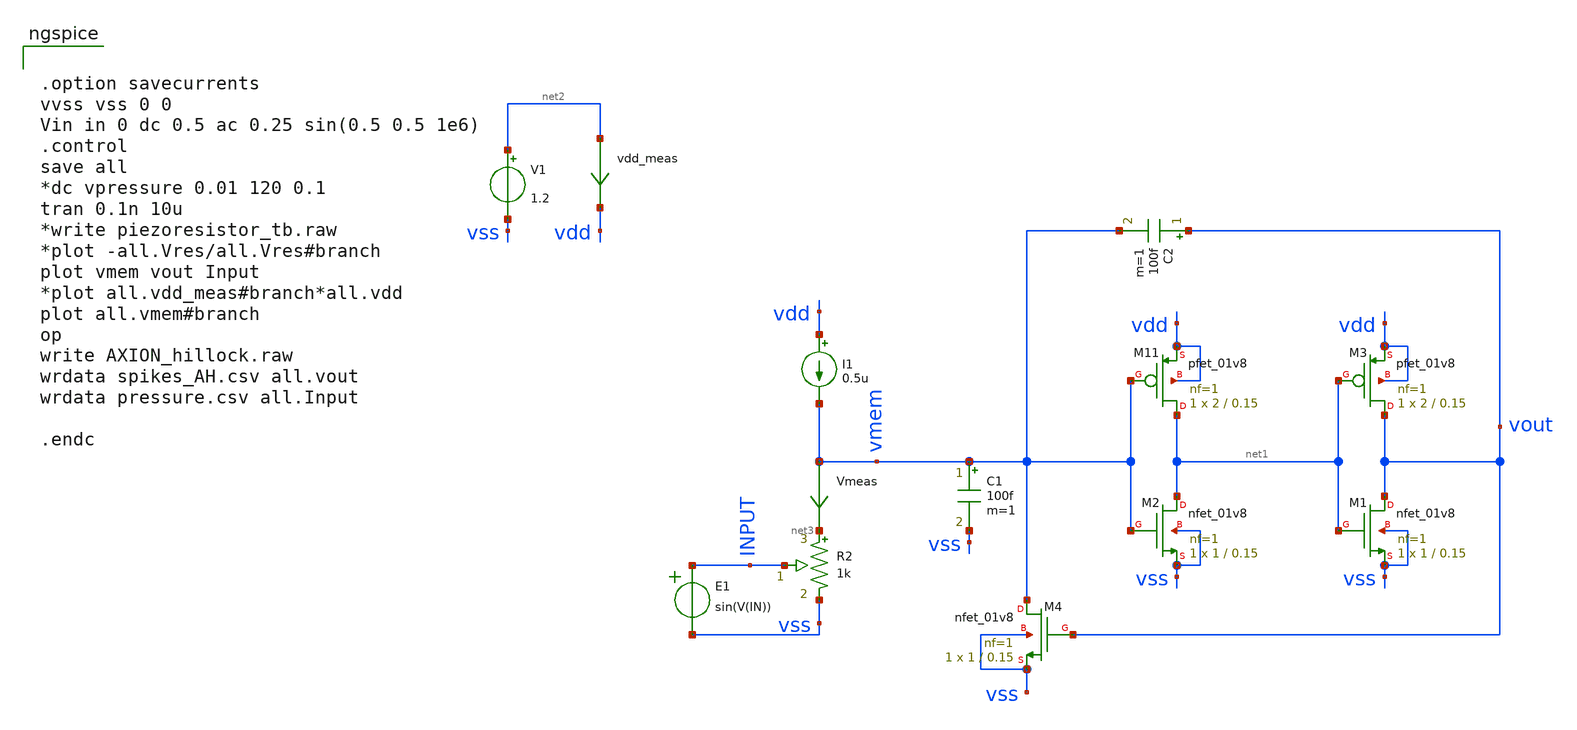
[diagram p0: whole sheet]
** sch_path: circuits/Axion_Hillock.sch
* Copyright 2020 Stefan Frederik Schippers
* Licensed under the Apache License, Version 2.0 (the "License");
* you may not use this file except in compliance with the License.
* You may obtain a copy of the License at
* https://www.apache.org/licenses/LICENSE-2.0
* Unless required by applicable law or agreed to in writing, software
* distributed under the License is distributed on an "AS IS" BASIS,
* WITHOUT WARRANTIES OR CONDITIONS OF ANY KIND, either express or implied.
* See the License for the specific language governing permissions and
* limitations under the License.
**.subckt Axion_Hillock
XM2 net1 vmem vss vss sky130_fd_pr__nfet_01v8 L=0.15 W=1 nf=1 ad='int((1 + 1)/2) * 1 / 1 * 0.29' as='int((1 + 2)/2) * 1 / 1 * 0.29'
+ pd='2*int((1 + 1)/2) * (1 / 1 + 0.29)' ps='2*int((1 + 2)/2) * (1 / 1 + 0.29)' nrd='0.29 / 1 ' nrs='0.29 / 1 '
+ sa=0 sb=0 sd=0 mult=1 m=1
XM11 net1 vmem vdd vdd sky130_fd_pr__pfet_01v8 L=0.15 W=2 nf=1 ad='int((nf+1)/2) * W/nf * 0.29' as='int((nf+2)/2) * W/nf * 0.29'
+ pd='2*int((nf+1)/2) * (W/nf + 0.29)' ps='2*int((nf+2)/2) * (W/nf + 0.29)' nrd='0.29 / W' nrs='0.29 / W'
+ sa=0 sb=0 sd=0 mult=1 m=1
XM1 vout net1 vss vss sky130_fd_pr__nfet_01v8 L=0.15 W=1 nf=1 ad='int((1 + 1)/2) * 1 / 1 * 0.29' as='int((1 + 2)/2) * 1 / 1 * 0.29'
+ pd='2*int((1 + 1)/2) * (1 / 1 + 0.29)' ps='2*int((1 + 2)/2) * (1 / 1 + 0.29)' nrd='0.29 / 1 ' nrs='0.29 / 1 '
+ sa=0 sb=0 sd=0 mult=1 m=1
XM3 vout net1 vdd vdd sky130_fd_pr__pfet_01v8 L=0.15 W=2 nf=1 ad='int((nf+1)/2) * W/nf * 0.29' as='int((nf+2)/2) * W/nf * 0.29'
+ pd='2*int((nf+1)/2) * (W/nf + 0.29)' ps='2*int((nf+2)/2) * (W/nf + 0.29)' nrd='0.29 / W' nrs='0.29 / W'
+ sa=0 sb=0 sd=0 mult=1 m=1
C1 vmem vss 100f m=1
I1 vdd vmem 0.5u
C2 vout vmem 100f m=1
XM4 vmem vout vss vss sky130_fd_pr__nfet_01v8 L=0.15 W=1 nf=1 ad='int((1 + 1)/2) * 1 / 1 * 0.29' as='int((1 + 2)/2) * 1 / 1 * 0.29'
+ pd='2*int((1 + 1)/2) * (1 / 1 + 0.29)' ps='2*int((1 + 2)/2) * (1 / 1 + 0.29)' nrd='0.29 / 1 ' nrs='0.29 / 1 '
+ sa=0 sb=0 sd=0 mult=1 m=1
R2 INPUT vss 1k m=5
E1 INPUT vss VOL=' sin(V(IN)) '
Vmeas vmem net3 0
.save i(vmeas)
vdd_meas net2 vdd 0
.save i(vdd_meas)
V1 net2 vss 1.2
**** begin user architecture code


.option savecurrents
vvss vss 0 0
Vin in 0 dc 0.5 ac 0.25 sin(0.5 0.5 1e6)
.control
save all
*dc vpressure 0.01 120 0.1
tran 0.1n 10u
*write piezoresistor_tb.raw
*plot -all.Vres/all.Vres#branch
plot vmem vout Input
*plot all.vdd_meas#branch*all.vdd
plot all.vmem#branch
op
write AXION_hillock.raw
wrdata spikes_AH.csv all.vout
wrdata pressure.csv all.Input

.endc


 .lib $::SKYWATER_MODELS/models/sky130.lib.spice tt

.param mc_mm_switch=0
.param mc_pr_switch=1


**** end user architecture code
**.ends
.end
